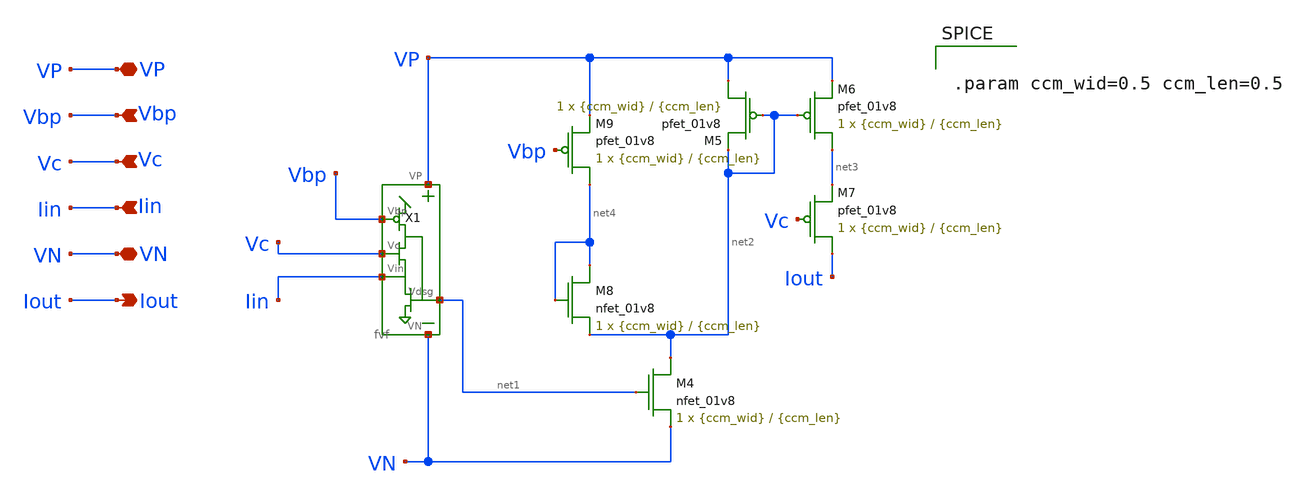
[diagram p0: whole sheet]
** sch_path: fvfccm.sch
**.subckt fvfccm Vbp Vc Iin VP VN Iout
*.ipin Vbp
*.ipin Vc
*.ipin Iin
*.iopin VP
*.iopin VN
*.opin Iout
XM4 net2 net1 VN VN sky130_fd_pr__nfet_01v8 L={ccm_len} W={ccm_wid} nf=1 ad='int((nf+1)/2) * W/nf * 0.29'
+ as='int((nf+2)/2) * W/nf * 0.29' pd='2*int((nf+1)/2) * (W/nf + 0.29)' ps='2*int((nf+2)/2) * (W/nf + 0.29)'
+ nrd='0.29 / W' nrs='0.29 / W' sa=0 sb=0 sd=0 mult=1 m=1
XM5 VP net2 net2 VP sky130_fd_pr__pfet_01v8 L={ccm_len} W={ccm_wid} nf=1 ad='int((nf+1)/2) * W/nf * 0.29'
+ as='int((nf+2)/2) * W/nf * 0.29' pd='2*int((nf+1)/2) * (W/nf + 0.29)' ps='2*int((nf+2)/2) * (W/nf + 0.29)'
+ nrd='0.29 / W' nrs='0.29 / W' sa=0 sb=0 sd=0 mult=1 m=1
XM6 net3 net2 VP VP sky130_fd_pr__pfet_01v8 L={ccm_len} W={ccm_wid} nf=1 ad='int((nf+1)/2) * W/nf * 0.29'
+ as='int((nf+2)/2) * W/nf * 0.29' pd='2*int((nf+1)/2) * (W/nf + 0.29)' ps='2*int((nf+2)/2) * (W/nf + 0.29)'
+ nrd='0.29 / W' nrs='0.29 / W' sa=0 sb=0 sd=0 mult=1 m=1
XM7 Iout Vc net3 VP sky130_fd_pr__pfet_01v8 L={ccm_len} W={ccm_wid} nf=1 ad='int((nf+1)/2) * W/nf * 0.29'
+ as='int((nf+2)/2) * W/nf * 0.29' pd='2*int((nf+1)/2) * (W/nf + 0.29)' ps='2*int((nf+2)/2) * (W/nf + 0.29)'
+ nrd='0.29 / W' nrs='0.29 / W' sa=0 sb=0 sd=0 mult=1 m=1
XM8 net4 net4 net2 VN sky130_fd_pr__nfet_01v8 L={ccm_len} W={ccm_wid} nf=1 ad='int((nf+1)/2) * W/nf * 0.29'
+ as='int((nf+2)/2) * W/nf * 0.29' pd='2*int((nf+1)/2) * (W/nf + 0.29)' ps='2*int((nf+2)/2) * (W/nf + 0.29)'
+ nrd='0.29 / W' nrs='0.29 / W' sa=0 sb=0 sd=0 mult=1 m=1
XM9 net4 Vbp VP VP sky130_fd_pr__pfet_01v8 L={ccm_len} W={ccm_wid} nf=1 ad='int((nf+1)/2) * W/nf * 0.29'
+ as='int((nf+2)/2) * W/nf * 0.29' pd='2*int((nf+1)/2) * (W/nf + 0.29)' ps='2*int((nf+2)/2) * (W/nf + 0.29)'
+ nrd='0.29 / W' nrs='0.29 / W' sa=0 sb=0 sd=0 mult=1 m=1
X1 VP Vbp Vc Iin net1 VN fvf
**** begin user architecture code


.param ccm_wid=0.5 ccm_len=0.5


**** end user architecture code
**.ends

* expanding   symbol:  fvf.sym # of pins=6
** sym_path: fvf.sym
** sch_path: fvf.sch
.subckt fvf VP Vbp Vc Vin Vdsg VN
*.iopin VP
*.iopin VN
*.ipin Vbp
*.ipin Vc
*.ipin Vin
*.opin Vdsg
XM1 VP Vbp Vdsg GND sky130_fd_pr__nfet_01v8 L=0.15 W=1 nf=1 ad='int((nf+1)/2) * W/nf * 0.29' as='int((nf+2)/2) * W/nf * 0.29'
+ pd='2*int((nf+1)/2) * (W/nf + 0.29)' ps='2*int((nf+2)/2) * (W/nf + 0.29)' nrd='0.29 / W' nrs='0.29 / W'
+ sa=0 sb=0 sd=0 mult=1 m=1
XM2 Vdsg Vc Vin GND sky130_fd_pr__nfet_01v8 L=0.15 W=1 nf=1 ad='int((nf+1)/2) * W/nf * 0.29' as='int((nf+2)/2) * W/nf * 0.29'
+ pd='2*int((nf+1)/2) * (W/nf + 0.29)' ps='2*int((nf+2)/2) * (W/nf + 0.29)' nrd='0.29 / W' nrs='0.29 / W'
+ sa=0 sb=0 sd=0 mult=1 m=1
XM3 Vdsg Vc Vin GND sky130_fd_pr__nfet_01v8 L=0.15 W=1 nf=1 ad='int((nf+1)/2) * W/nf * 0.29' as='int((nf+2)/2) * W/nf * 0.29'
+ pd='2*int((nf+1)/2) * (W/nf + 0.29)' ps='2*int((nf+2)/2) * (W/nf + 0.29)' nrd='0.29 / W' nrs='0.29 / W'
+ sa=0 sb=0 sd=0 mult=1 m=1
XM4 VN Vdsg Vin GND sky130_fd_pr__nfet_01v8 L=0.15 W=1 nf=1 ad='int((nf+1)/2) * W/nf * 0.29' as='int((nf+2)/2) * W/nf * 0.29'
+ pd='2*int((nf+1)/2) * (W/nf + 0.29)' ps='2*int((nf+2)/2) * (W/nf + 0.29)' nrd='0.29 / W' nrs='0.29 / W'
+ sa=0 sb=0 sd=0 mult=1 m=1
.ends

.end
